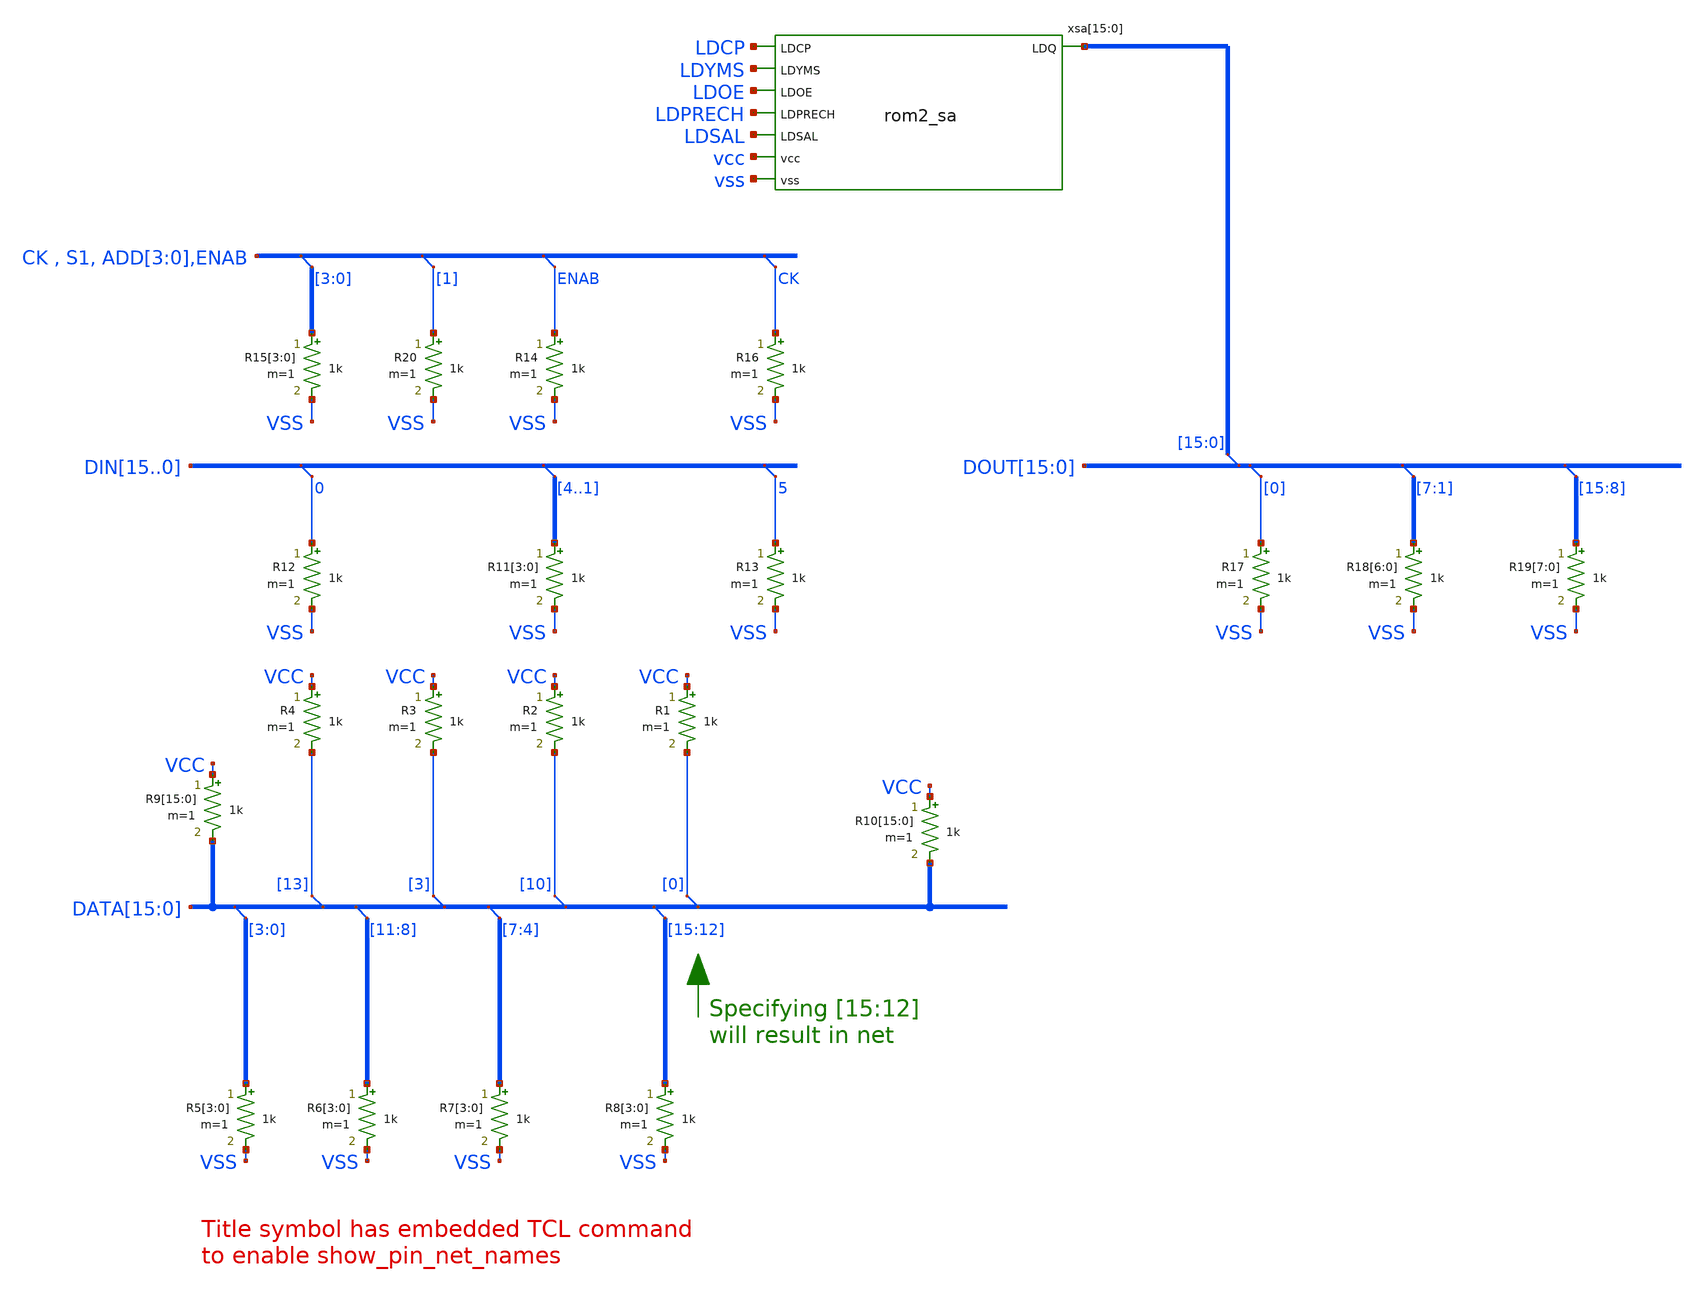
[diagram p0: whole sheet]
** sch_path: xschem-src/xschem_library/examples/test_bus_tap.sch
* Copyright (C) 1998-2026 Stefan Frederik Schippers
* This program is free software; you can redistribute it and/or modify
* it under the terms of the GNU General Public License as published by
* the Free Software Foundation; either version 2 of the License, or
* (at your option) any later version.
* This program is distributed in the hope that it will be useful,
* but WITHOUT ANY WARRANTY; without even the implied warranty of
* MERCHANTABILITY or FITNESS FOR A PARTICULAR PURPOSE.  See the
* GNU General Public License for more details.
* You should have received a copy of the GNU General Public License
* along with this program; if not, write to the Free Software
**.subckt test_bus_tap
* tap: DATA[15:0] --> DATA[3]
* tap: DATA[15:0] --> DATA[13]
* tap: DATA[15:0] --> DATA[7:4]
* tap: DATA[15:0] --> DATA[11:8]
* tap: DATA[15:0] --> DATA[3:0]
* tap: DATA[15:0] --> DATA[10]
* tap: DATA[15:0] --> DATA[0]
R1 VCC DATA[0] 1k m=1
R2 VCC DATA[10] 1k m=1
R3 VCC DATA[3] 1k m=1
R4 VCC DATA[13] 1k m=1
R5[3] DATA[3] VSS 1k m=1
R5[2] DATA[2] VSS 1k m=1
R5[1] DATA[1] VSS 1k m=1
R5[0] DATA[0] VSS 1k m=1
R6[3] DATA[11] VSS 1k m=1
R6[2] DATA[10] VSS 1k m=1
R6[1] DATA[9] VSS 1k m=1
R6[0] DATA[8] VSS 1k m=1
R7[3] DATA[7] VSS 1k m=1
R7[2] DATA[6] VSS 1k m=1
R7[1] DATA[5] VSS 1k m=1
R7[0] DATA[4] VSS 1k m=1
R8[3] DATA[15] VSS 1k m=1
R8[2] DATA[14] VSS 1k m=1
R8[1] DATA[13] VSS 1k m=1
R8[0] DATA[12] VSS 1k m=1
* tap: DATA[15:0] --> DATA[15:12]
R9[15] VCC DATA[15] 1k m=1
R9[14] VCC DATA[14] 1k m=1
R9[13] VCC DATA[13] 1k m=1
R9[12] VCC DATA[12] 1k m=1
R9[11] VCC DATA[11] 1k m=1
R9[10] VCC DATA[10] 1k m=1
R9[9] VCC DATA[9] 1k m=1
R9[8] VCC DATA[8] 1k m=1
R9[7] VCC DATA[7] 1k m=1
R9[6] VCC DATA[6] 1k m=1
R9[5] VCC DATA[5] 1k m=1
R9[4] VCC DATA[4] 1k m=1
R9[3] VCC DATA[3] 1k m=1
R9[2] VCC DATA[2] 1k m=1
R9[1] VCC DATA[1] 1k m=1
R9[0] VCC DATA[0] 1k m=1
R10[15] VCC DATA[15] 1k m=1
R10[14] VCC DATA[14] 1k m=1
R10[13] VCC DATA[13] 1k m=1
R10[12] VCC DATA[12] 1k m=1
R10[11] VCC DATA[11] 1k m=1
R10[10] VCC DATA[10] 1k m=1
R10[9] VCC DATA[9] 1k m=1
R10[8] VCC DATA[8] 1k m=1
R10[7] VCC DATA[7] 1k m=1
R10[6] VCC DATA[6] 1k m=1
R10[5] VCC DATA[5] 1k m=1
R10[4] VCC DATA[4] 1k m=1
R10[3] VCC DATA[3] 1k m=1
R10[2] VCC DATA[2] 1k m=1
R10[1] VCC DATA[1] 1k m=1
R10[0] VCC DATA[0] 1k m=1
* tap: DIN[15..0] --> DIN0
* tap: DIN[15..0] --> DIN[4..1]
R11[3] DIN4 VSS 1k m=1
R11[2] DIN3 VSS 1k m=1
R11[1] DIN2 VSS 1k m=1
R11[0] DIN1 VSS 1k m=1
R12 DIN0 VSS 1k m=1
* tap: DIN[15..0] --> DIN5
R13 DIN5 VSS 1k m=1
* tap: CK , S1, ADD[3:0],ENAB --> ADD[3:0]
* tap: CK , S1, ADD[3:0],ENAB --> ENAB
R15[3] ADD[3] VSS 1k m=1
R15[2] ADD[2] VSS 1k m=1
R15[1] ADD[1] VSS 1k m=1
R15[0] ADD[0] VSS 1k m=1
R14 ENAB VSS 1k m=1
* tap: CK , S1, ADD[3:0],ENAB --> CK
R16 CK VSS 1k m=1
* tap: DOUT[15:0] --> DOUT[0]
* tap: DOUT[15:0] --> DOUT[7:1]
R18[6] DOUT[7] VSS 1k m=1
R18[5] DOUT[6] VSS 1k m=1
R18[4] DOUT[5] VSS 1k m=1
R18[3] DOUT[4] VSS 1k m=1
R18[2] DOUT[3] VSS 1k m=1
R18[1] DOUT[2] VSS 1k m=1
R18[0] DOUT[1] VSS 1k m=1
R17 DOUT[0] VSS 1k m=1
* tap: DOUT[15:0] --> DOUT[15:8]
R19[7] DOUT[15] VSS 1k m=1
R19[6] DOUT[14] VSS 1k m=1
R19[5] DOUT[13] VSS 1k m=1
R19[4] DOUT[12] VSS 1k m=1
R19[3] DOUT[11] VSS 1k m=1
R19[2] DOUT[10] VSS 1k m=1
R19[1] DOUT[9] VSS 1k m=1
R19[0] DOUT[8] VSS 1k m=1
xsa[15] DOUT[15] LDCP LDYMS LDOE LDPRECH LDSAL vcc vss rom2_sa
xsa[14] DOUT[14] LDCP LDYMS LDOE LDPRECH LDSAL vcc vss rom2_sa
xsa[13] DOUT[13] LDCP LDYMS LDOE LDPRECH LDSAL vcc vss rom2_sa
xsa[12] DOUT[12] LDCP LDYMS LDOE LDPRECH LDSAL vcc vss rom2_sa
xsa[11] DOUT[11] LDCP LDYMS LDOE LDPRECH LDSAL vcc vss rom2_sa
xsa[10] DOUT[10] LDCP LDYMS LDOE LDPRECH LDSAL vcc vss rom2_sa
xsa[9] DOUT[9] LDCP LDYMS LDOE LDPRECH LDSAL vcc vss rom2_sa
xsa[8] DOUT[8] LDCP LDYMS LDOE LDPRECH LDSAL vcc vss rom2_sa
xsa[7] DOUT[7] LDCP LDYMS LDOE LDPRECH LDSAL vcc vss rom2_sa
xsa[6] DOUT[6] LDCP LDYMS LDOE LDPRECH LDSAL vcc vss rom2_sa
xsa[5] DOUT[5] LDCP LDYMS LDOE LDPRECH LDSAL vcc vss rom2_sa
xsa[4] DOUT[4] LDCP LDYMS LDOE LDPRECH LDSAL vcc vss rom2_sa
xsa[3] DOUT[3] LDCP LDYMS LDOE LDPRECH LDSAL vcc vss rom2_sa
xsa[2] DOUT[2] LDCP LDYMS LDOE LDPRECH LDSAL vcc vss rom2_sa
xsa[1] DOUT[1] LDCP LDYMS LDOE LDPRECH LDSAL vcc vss rom2_sa
xsa[0] DOUT[0] LDCP LDYMS LDOE LDPRECH LDSAL vcc vss rom2_sa
* tap: DOUT[15:0] --> DOUT[15:0]
* tap: CK , S1, ADD[3:0],ENAB --> ADD[1]
R20 ADD[1] VSS 1k m=1
**.ends

* expanding   symbol:  rom2_sa.sym # of pins=8
** sym_path: xschem-src/xschem_library/rom8k/rom2_sa.sym
** sch_path: xschem-src/xschem_library/rom8k/rom2_sa.sch
.subckt rom2_sa LDQ LDCP LDYMS LDOE LDPRECH LDSAL vcc vss
*.opin LDQ
*.ipin LDCP
*.ipin LDYMS
*.ipin LDOE
*.ipin LDPRECH
*.ipin LDSAL
*.ipin vcc
*.ipin vss
x242 LDSALI LDSALI_B vcc vss lvnot wn=8.4u lln=2.4u wp=12u lp=2.4u m=1
x249 LDCP_B LDCP vcc vss lvnot wn=8.4u lln=2.4u wp=20u lp=2.4u m=1
x6 LDQ LDQIII LDOE vcc vss bts
x7 net1 LDQII LDSALI LDSALI_B vcc vss passhs WN=12u LN=1.2u WP=12u LP=1.2u
m6 LDQII LDQIB net2 0 cmosn w=24u l=2.4u ad={24u *4.4u} as={24u *4.4u} pd={24u *2 + 8.8u} ps={24u *2 + 8.8u}
+ m=1
m7 LDQII LDQIB net3 VCC cmosp w=24u l=2.4u ad={24u *4.4u} as={24u *4.4u} pd={24u *2 + 8.8u} ps={24u *2 + 8.8u}
+ m=1
m4 net2 LDSALI vss 0 cmosn w=24u l=2.4u ad={24u *4.4u} as={24u *4.4u} pd={24u *2 + 8.8u} ps={24u *2 + 8.8u}
+ m=1
m1 net3 LDSALI_B vcc VCC cmosp w=24u l=2.4u ad={24u *4.4u} as={24u *4.4u} pd={24u *2 + 8.8u} ps={24u *2 + 8.8u}
+ m=1
x8 net4 LDQII vcc vss lvnot wn=8.4u lln=2.4u wp=12u lp=2.4u m=1
x9 net1 net4 vcc vss lvnot wn=8.4u lln=2.4u wp=12u lp=2.4u m=1
c0 LDQII vss 3f m=1
c1 LDQIB vss 3f m=1
x228 LDQIII LDQII vcc vss lvnot wn=24u lln=2.4u wp=60u lp=2.4u m=1
x1 LDSALI_B LDSAL vcc vss lvnot wn=8.4u lln=2.4u wp=12u lp=2.4u m=1
xsacell LDCP_B LDPRECH vcc vss LDQI LDQIB LDYMS rom2_sacell
.save v(ldqib)
.save v(ldqii)
.save v(ldcp_b)
.save v(ldsali)
.save v(ldqi)
.save v(ldqiii)
.ends


* expanding   symbol:  lvnot.sym # of pins=2
** sym_path: xschem-src/xschem_library/rom8k/lvnot.sym
** sch_path: xschem-src/xschem_library/rom8k/lvnot.sch
.subckt lvnot y a VCCPIN VSSPIN     wn=10u lln=1.2u wp=10u lp=1.2u
*.opin y
*.ipin a
m2 DP a VCCPIN VCCPIN cmosp w=wp l=lp ad='wp *4.6u' as='wp *4.6u' pd='wp *2+9.2u' ps='wp *2+9.2u' m=1
m1 DN a VSSPIN VSSPIN cmosn w=wn l=lln ad='wn *4.3u' as='wn *4.3u' pd='wn *2+8.6u' ps='wn *2+8.6u' m=1
Vmeas DP y 0
.save i(vmeas)
Vmeas1 y DN 0
.save i(vmeas1)
.save v(dp)
.save v(dn)
.ends


* expanding   symbol:  bts.sym # of pins=3
** sym_path: xschem-src/xschem_library/rom8k/bts.sym
** sch_path: xschem-src/xschem_library/rom8k/bts.sch
.subckt bts Z A E VCCPIN VSSPIN
*.ipin A
*.ipin E
*.opin Z
m7 NN EN PP VCCPIN cmosp w=56u l=2.4u ad={56u *2.2u} as={56u *2.2u} pd={56u *2+4.4u} ps={56u *2+4.4u}
+ m=1
m8 PP A VCCPIN VCCPIN cmosp w=56u l=2.4u ad={56u *2.2u} as={56u *2.2u} pd={56u *2+4.4u} ps={56u *2+4.4u}
+ m=1
m9 NN A VSSPIN 0 cmosn w=20u l=2.4u ad={20u *4.4u} as={20u *4.4u} pd={20u *2 + 8.8u} ps={20u *2 + 8.8u}
+ m=1
m1 PP E NN 0 cmosn w=24u l=2.4u ad={24u *4.4u} as={24u *4.4u} pd={24u *2 + 8.8u} ps={24u *2 + 8.8u} m=1
m11 Z PP VCCPIN VCCPIN cmosp w=200u l=2.4u ad={200u *2.2u} as={200u *2.2u} pd={200u *2+4.4u} ps={200u *2+4.4u}
+ m=1
m12 Z NN VSSPIN 0 cmosn w=80u l=2.4u ad={80u *4.4u} as={80u *4.4u} pd={80u *2 + 8.8u} ps={80u *2 + 8.8u}
+ m=1
m13 NN EN VSSPIN 0 cmosn w=20u l=2.4u ad={20u *4.4u} as={20u *4.4u} pd={20u *2 + 8.8u} ps={20u *2 + 8.8u}
+ m=1
m14 PP E VCCPIN VCCPIN cmosp w=50u l=2.4u ad={50u *2.2u} as={50u *2.2u} pd={50u *2+4.4u} ps={50u *2+4.4u}
+ m=1
m15 EN E VCCPIN VCCPIN cmosp w=50u l=2.4u ad={50u *2.2u} as={50u *2.2u} pd={50u *2+4.4u} ps={50u *2+4.4u}
+ m=1
m16 EN E VSSPIN 0 cmosn w=20u l=2.4u ad={20u *4.4u} as={20u *4.4u} pd={20u *2 + 8.8u} ps={20u *2 + 8.8u}
+ m=1
c0 E VSSPIN 3f m=1
c4 NN VSSPIN 3f m=1
c5 PP VSSPIN 3f m=1
c6 EN VSSPIN 3f m=1
.ends


* expanding   symbol:  passhs.sym # of pins=4
** sym_path: xschem-src/xschem_library/rom8k/passhs.sym
** sch_path: xschem-src/xschem_library/rom8k/passhs.sch
.subckt passhs Z A EN E VCCPIN VSSPIN  WN=2u LN=1.2u WP=2u LP=1.2u
*.iopin Z
*.iopin A
*.ipin EN
*.ipin E
m60 Z EN A VCCPIN cmosp w=WP l=2.4u ad='WP *4.6u' as='WP *4.6u' pd='WP *2+9.2u' ps='WP *2+9.2u' m=1
m1 A E Z VSSPIN cmosn w=WN l=2.4u ad='WN *4.3u' as='WN *4.3u' pd='WN *2+8.6u' ps='WN *2+8.6u' m=1
* noconn VSSPIN
* noconn VCCPIN
.ends


* expanding   symbol:  rom2_sacell.sym # of pins=7
** sym_path: xschem-src/xschem_library/rom8k/rom2_sacell.sym
** sch_path: xschem-src/xschem_library/rom8k/rom2_sacell.sch
.subckt rom2_sacell LDRESET LDPRECH VCC VSS LDQI LDQ_B LDYMS
*.ipin LDRESET
*.ipin LDPRECH
*.ipin VCC
*.ipin VSS
*.opin LDQI
*.opin LDQ_B
*.iopin LDYMS
m3 VCC LDPRECH LDYMS VSS cmosn w=WPRECH l=2u ad='WPRECH *4.3u' as='WPRECH *4.3u' pd='WPRECH *2+8.6u'
+ ps='WPRECH *2+8.6u' m=10
m1 LDQI VCC LDYMS VSS cmosn w=WPRECH l=2u ad='WPRECH *4.3u' as='WPRECH *4.3u' pd='WPRECH *2+8.6u' ps='WPRECH *2+8.6u'
+ m=2
m5 LDQI LDRESET VCC VCC cmosp w=6.6u l=8.8u ad={6.6u *4.4u} as={6.6u *4.4u} pd={6.6u *2 + 8.8u} ps={6.6u *2 + 8.8u}
+ m=1
m11 LDYMS LDRESET VSS 0 cmosn w=16u l=2.4u ad={16u *4.4u} as={16u *4.4u} pd={16u *2 + 8.8u} ps={16u *2 + 8.8u}
+ m=1
c2 LDQI VSS 3f m=1
m2 LDQ_B LDQI VSS 0 cmosn w=8u l=2.4u ad={8u *4.4u} as={8u *4.4u} pd={8u *2 + 8.8u} ps={8u *2 + 8.8u}
+ m=1
m4 LDQ_B LDQI VCC VCC cmosp w=40u l=2.4u ad='40u *4.6u' as='40u *4.6u' pd='40u *2+9.2u' ps='40u *2+9.2u'
+ m=1
.ends

.end
